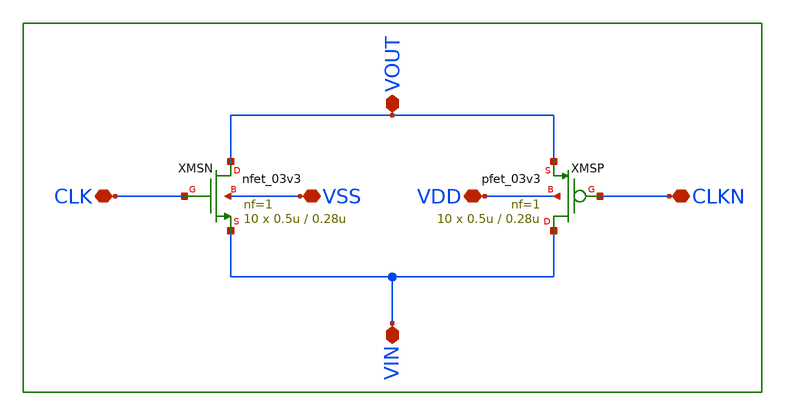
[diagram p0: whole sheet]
** sch_path: designs/sar_adc/dac/dac_sw_1state_B/xschem/dac_sw_1state_B.sch
**.subckt dac_sw_1state_B VIN VOUT CLK CLKN VSS VDD
*.iopin VIN
*.iopin VOUT
*.iopin CLK
*.iopin CLKN
*.iopin VSS
*.iopin VDD
XMSN VOUT CLK VIN VSS nfet_03v3 L=0.28u W=0.5u nf=1 ad='int((nf+1)/2) * W/nf * 0.18u' as='int((nf+2)/2) * W/nf * 0.18u'
+ pd='2*int((nf+1)/2) * (W/nf + 0.18u)' ps='2*int((nf+2)/2) * (W/nf + 0.18u)' nrd='0.18u / W' nrs='0.18u / W'
+ sa=0 sb=0 sd=0 m=10
XMSP VIN CLKN VOUT VDD pfet_03v3 L=0.28u W=0.5u nf=1 ad='int((nf+1)/2) * W/nf * 0.18u' as='int((nf+2)/2) * W/nf * 0.18u'
+ pd='2*int((nf+1)/2) * (W/nf + 0.18u)' ps='2*int((nf+2)/2) * (W/nf + 0.18u)' nrd='0.18u / W' nrs='0.18u / W'
+ sa=0 sb=0 sd=0 m=10
**.ends
.end
